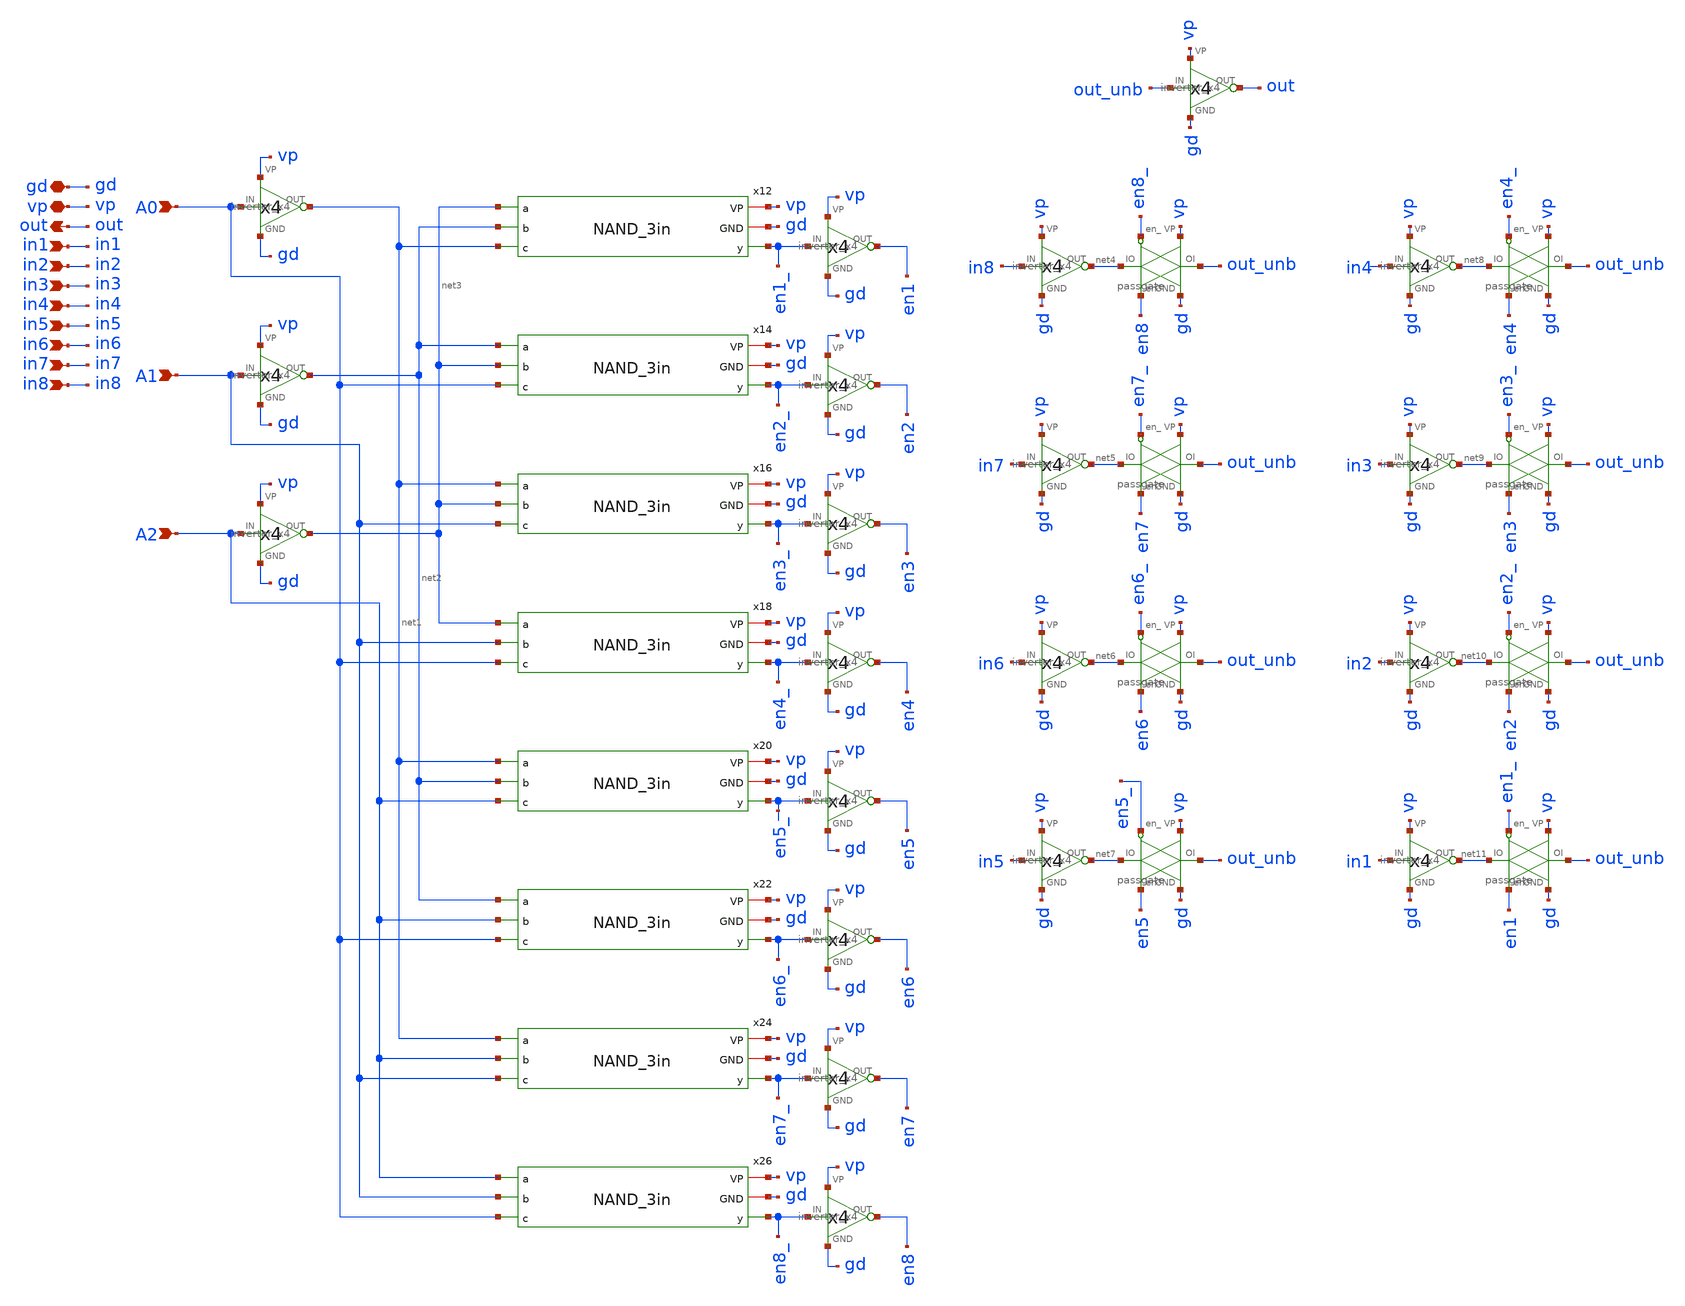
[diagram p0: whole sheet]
** sch_path: schematics/divider/schematics/MUX_8to1.sch
**.subckt MUX_8to1 gd vp out in1 in2 in3 in4 in5 in6 in7 in8 A0 A1 A2
*.iopin gd
*.iopin vp
*.opin out
*.ipin in1
*.ipin in2
*.ipin in3
*.ipin in4
*.ipin in5
*.ipin in6
*.ipin in7
*.ipin in8
*.ipin A0
*.ipin A1
*.ipin A2
x9 A0 net1 vp gd inverter_x4
x10 A1 net2 vp gd inverter_x4
x11 A2 net3 vp gd inverter_x4
x28 out_unb out vp gd inverter_x4
x29 in4 net8 vp gd inverter_x4
x30 in8 net4 vp gd inverter_x4
x31 in7 net5 vp gd inverter_x4
x32 in6 net6 vp gd inverter_x4
x33 in5 net7 vp gd inverter_x4
x34 in1 net11 vp gd inverter_x4
x35 in2 net10 vp gd inverter_x4
x36 in3 net9 vp gd inverter_x4
x13 en1_ en1 vp gd inverter_x4
x15 en2_ en2 vp gd inverter_x4
x17 en3_ en3 vp gd inverter_x4
x19 en4_ en4 vp gd inverter_x4
x21 en5_ en5 vp gd inverter_x4
x23 en6_ en6 vp gd inverter_x4
x25 en7_ en7 vp gd inverter_x4
x27 en8_ en8 vp gd inverter_x4
x12 vp gd net3 en1_ net2 net1 NAND_3in
x14 vp gd net2 en2_ net3 A0 NAND_3in
x16 vp gd net1 en3_ net3 A1 NAND_3in
x18 vp gd net3 en4_ A1 A0 NAND_3in
x20 vp gd net1 en5_ net2 A2 NAND_3in
x22 vp gd net2 en6_ A2 A0 NAND_3in
x24 vp gd net1 en7_ A2 A1 NAND_3in
x26 vp gd A2 en8_ A1 A0 NAND_3in
x1 en8_ vp gd en8 net4 out_unb passgate
x2 en4_ vp gd en4 net8 out_unb passgate
x3 en7_ vp gd en7 net5 out_unb passgate
x4 en3_ vp gd en3 net9 out_unb passgate
x5 en6_ vp gd en6 net6 out_unb passgate
x6 en2_ vp gd en2 net10 out_unb passgate
x7 en5_ vp gd en5 net7 out_unb passgate
x8 en1_ vp gd en1 net11 out_unb passgate
**.ends
.end
